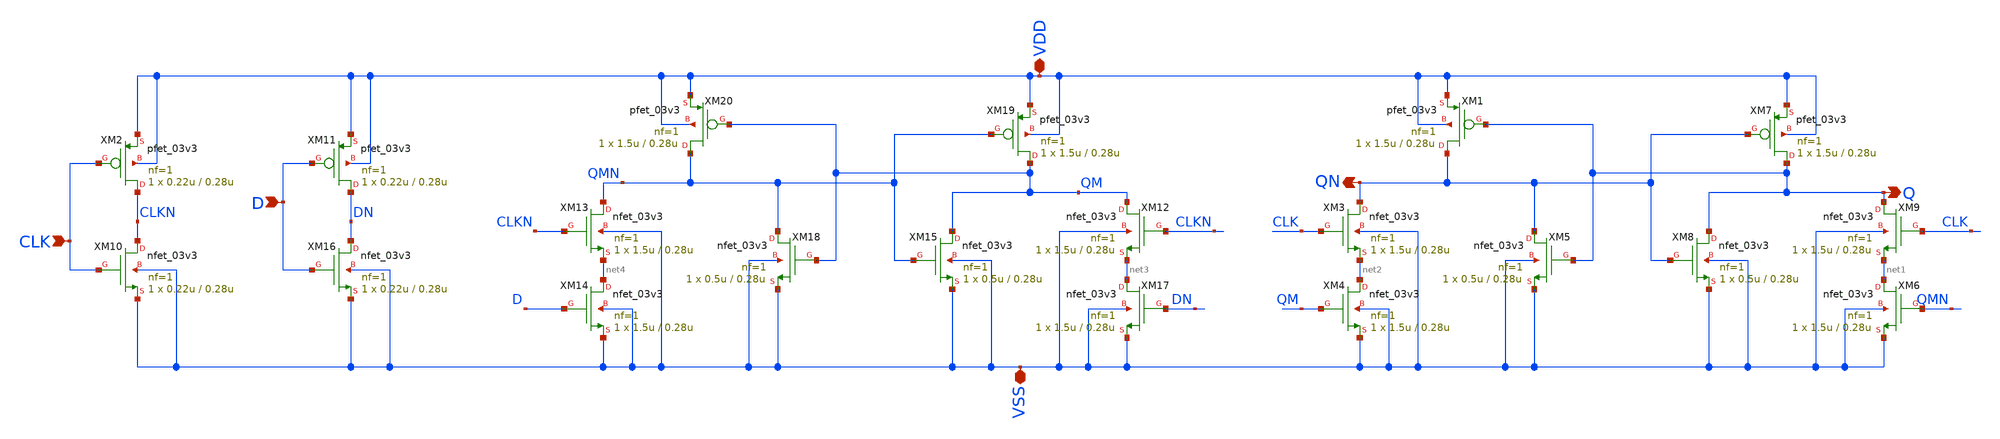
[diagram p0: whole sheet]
** sch_path: designs/DS_modulator/dff/xschem/dff.sch
**.subckt dff CLK QN Q D VDD VSS
*.ipin CLK
*.opin QN
*.opin Q
*.ipin D
*.iopin VDD
*.iopin VSS
XM2 CLKN CLK VDD VDD pfet_03v3 L=0.28u W=0.22u nf=1 ad='int((nf+1)/2) * W/nf * 0.18u' as='int((nf+2)/2) * W/nf * 0.18u'
+ pd='2*int((nf+1)/2) * (W/nf + 0.18u)' ps='2*int((nf+2)/2) * (W/nf + 0.18u)' nrd='0.18u / W' nrs='0.18u / W'
+ sa=0 sb=0 sd=0 m=1
XM9 Q CLK net1 VSS nfet_03v3 L=0.28u W=1.5u nf=1 ad='int((nf+1)/2) * W/nf * 0.18u' as='int((nf+2)/2) * W/nf * 0.18u'
+ pd='2*int((nf+1)/2) * (W/nf + 0.18u)' ps='2*int((nf+2)/2) * (W/nf + 0.18u)' nrd='0.18u / W' nrs='0.18u / W'
+ sa=0 sb=0 sd=0 m=1
XM3 QN CLK net2 VSS nfet_03v3 L=0.28u W=1.5u nf=1 ad='int((nf+1)/2) * W/nf * 0.18u' as='int((nf+2)/2) * W/nf * 0.18u'
+ pd='2*int((nf+1)/2) * (W/nf + 0.18u)' ps='2*int((nf+2)/2) * (W/nf + 0.18u)' nrd='0.18u / W' nrs='0.18u / W'
+ sa=0 sb=0 sd=0 m=1
XM4 net2 QM VSS VSS nfet_03v3 L=0.28u W=1.5u nf=1 ad='int((nf+1)/2) * W/nf * 0.18u' as='int((nf+2)/2) * W/nf * 0.18u'
+ pd='2*int((nf+1)/2) * (W/nf + 0.18u)' ps='2*int((nf+2)/2) * (W/nf + 0.18u)' nrd='0.18u / W' nrs='0.18u / W'
+ sa=0 sb=0 sd=0 m=1
XM8 Q QN VSS VSS nfet_03v3 L=0.28u W=0.5u nf=1 ad='int((nf+1)/2) * W/nf * 0.18u' as='int((nf+2)/2) * W/nf * 0.18u'
+ pd='2*int((nf+1)/2) * (W/nf + 0.18u)' ps='2*int((nf+2)/2) * (W/nf + 0.18u)' nrd='0.18u / W' nrs='0.18u / W'
+ sa=0 sb=0 sd=0 m=1
XM10 CLKN CLK VSS VSS nfet_03v3 L=0.28u W=0.22u nf=1 ad='int((nf+1)/2) * W/nf * 0.18u' as='int((nf+2)/2) * W/nf * 0.18u'
+ pd='2*int((nf+1)/2) * (W/nf + 0.18u)' ps='2*int((nf+2)/2) * (W/nf + 0.18u)' nrd='0.18u / W' nrs='0.18u / W'
+ sa=0 sb=0 sd=0 m=1
XM6 net1 QMN VSS VSS nfet_03v3 L=0.28u W=1.5u nf=1 ad='int((nf+1)/2) * W/nf * 0.18u' as='int((nf+2)/2) * W/nf * 0.18u'
+ pd='2*int((nf+1)/2) * (W/nf + 0.18u)' ps='2*int((nf+2)/2) * (W/nf + 0.18u)' nrd='0.18u / W' nrs='0.18u / W'
+ sa=0 sb=0 sd=0 m=1
XM5 QN Q VSS VSS nfet_03v3 L=0.28u W=0.5u nf=1 ad='int((nf+1)/2) * W/nf * 0.18u' as='int((nf+2)/2) * W/nf * 0.18u'
+ pd='2*int((nf+1)/2) * (W/nf + 0.18u)' ps='2*int((nf+2)/2) * (W/nf + 0.18u)' nrd='0.18u / W' nrs='0.18u / W'
+ sa=0 sb=0 sd=0 m=1
XM7 Q QN VDD VDD pfet_03v3 L=0.28u W=1.5u nf=1 ad='int((nf+1)/2) * W/nf * 0.18u' as='int((nf+2)/2) * W/nf * 0.18u'
+ pd='2*int((nf+1)/2) * (W/nf + 0.18u)' ps='2*int((nf+2)/2) * (W/nf + 0.18u)' nrd='0.18u / W' nrs='0.18u / W'
+ sa=0 sb=0 sd=0 m=1
XM1 QN Q VDD VDD pfet_03v3 L=0.28u W=1.5u nf=1 ad='int((nf+1)/2) * W/nf * 0.18u' as='int((nf+2)/2) * W/nf * 0.18u'
+ pd='2*int((nf+1)/2) * (W/nf + 0.18u)' ps='2*int((nf+2)/2) * (W/nf + 0.18u)' nrd='0.18u / W' nrs='0.18u / W'
+ sa=0 sb=0 sd=0 m=1
XM11 DN D VDD VDD pfet_03v3 L=0.28u W=0.22u nf=1 ad='int((nf+1)/2) * W/nf * 0.18u' as='int((nf+2)/2) * W/nf * 0.18u'
+ pd='2*int((nf+1)/2) * (W/nf + 0.18u)' ps='2*int((nf+2)/2) * (W/nf + 0.18u)' nrd='0.18u / W' nrs='0.18u / W'
+ sa=0 sb=0 sd=0 m=1
XM12 QM CLKN net3 VSS nfet_03v3 L=0.28u W=1.5u nf=1 ad='int((nf+1)/2) * W/nf * 0.18u' as='int((nf+2)/2) * W/nf * 0.18u'
+ pd='2*int((nf+1)/2) * (W/nf + 0.18u)' ps='2*int((nf+2)/2) * (W/nf + 0.18u)' nrd='0.18u / W' nrs='0.18u / W'
+ sa=0 sb=0 sd=0 m=1
XM13 QMN CLKN net4 VSS nfet_03v3 L=0.28u W=1.5u nf=1 ad='int((nf+1)/2) * W/nf * 0.18u' as='int((nf+2)/2) * W/nf * 0.18u'
+ pd='2*int((nf+1)/2) * (W/nf + 0.18u)' ps='2*int((nf+2)/2) * (W/nf + 0.18u)' nrd='0.18u / W' nrs='0.18u / W'
+ sa=0 sb=0 sd=0 m=1
XM14 net4 D VSS VSS nfet_03v3 L=0.28u W=1.5u nf=1 ad='int((nf+1)/2) * W/nf * 0.18u' as='int((nf+2)/2) * W/nf * 0.18u'
+ pd='2*int((nf+1)/2) * (W/nf + 0.18u)' ps='2*int((nf+2)/2) * (W/nf + 0.18u)' nrd='0.18u / W' nrs='0.18u / W'
+ sa=0 sb=0 sd=0 m=1
XM15 QM QMN VSS VSS nfet_03v3 L=0.28u W=0.5u nf=1 ad='int((nf+1)/2) * W/nf * 0.18u' as='int((nf+2)/2) * W/nf * 0.18u'
+ pd='2*int((nf+1)/2) * (W/nf + 0.18u)' ps='2*int((nf+2)/2) * (W/nf + 0.18u)' nrd='0.18u / W' nrs='0.18u / W'
+ sa=0 sb=0 sd=0 m=1
XM16 DN D VSS VSS nfet_03v3 L=0.28u W=0.22u nf=1 ad='int((nf+1)/2) * W/nf * 0.18u' as='int((nf+2)/2) * W/nf * 0.18u'
+ pd='2*int((nf+1)/2) * (W/nf + 0.18u)' ps='2*int((nf+2)/2) * (W/nf + 0.18u)' nrd='0.18u / W' nrs='0.18u / W'
+ sa=0 sb=0 sd=0 m=1
XM17 net3 DN VSS VSS nfet_03v3 L=0.28u W=1.5u nf=1 ad='int((nf+1)/2) * W/nf * 0.18u' as='int((nf+2)/2) * W/nf * 0.18u'
+ pd='2*int((nf+1)/2) * (W/nf + 0.18u)' ps='2*int((nf+2)/2) * (W/nf + 0.18u)' nrd='0.18u / W' nrs='0.18u / W'
+ sa=0 sb=0 sd=0 m=1
XM18 QMN QM VSS VSS nfet_03v3 L=0.28u W=0.5u nf=1 ad='int((nf+1)/2) * W/nf * 0.18u' as='int((nf+2)/2) * W/nf * 0.18u'
+ pd='2*int((nf+1)/2) * (W/nf + 0.18u)' ps='2*int((nf+2)/2) * (W/nf + 0.18u)' nrd='0.18u / W' nrs='0.18u / W'
+ sa=0 sb=0 sd=0 m=1
XM19 QM QMN VDD VDD pfet_03v3 L=0.28u W=1.5u nf=1 ad='int((nf+1)/2) * W/nf * 0.18u' as='int((nf+2)/2) * W/nf * 0.18u'
+ pd='2*int((nf+1)/2) * (W/nf + 0.18u)' ps='2*int((nf+2)/2) * (W/nf + 0.18u)' nrd='0.18u / W' nrs='0.18u / W'
+ sa=0 sb=0 sd=0 m=1
XM20 QMN QM VDD VDD pfet_03v3 L=0.28u W=1.5u nf=1 ad='int((nf+1)/2) * W/nf * 0.18u' as='int((nf+2)/2) * W/nf * 0.18u'
+ pd='2*int((nf+1)/2) * (W/nf + 0.18u)' ps='2*int((nf+2)/2) * (W/nf + 0.18u)' nrd='0.18u / W' nrs='0.18u / W'
+ sa=0 sb=0 sd=0 m=1
**.ends
.end
